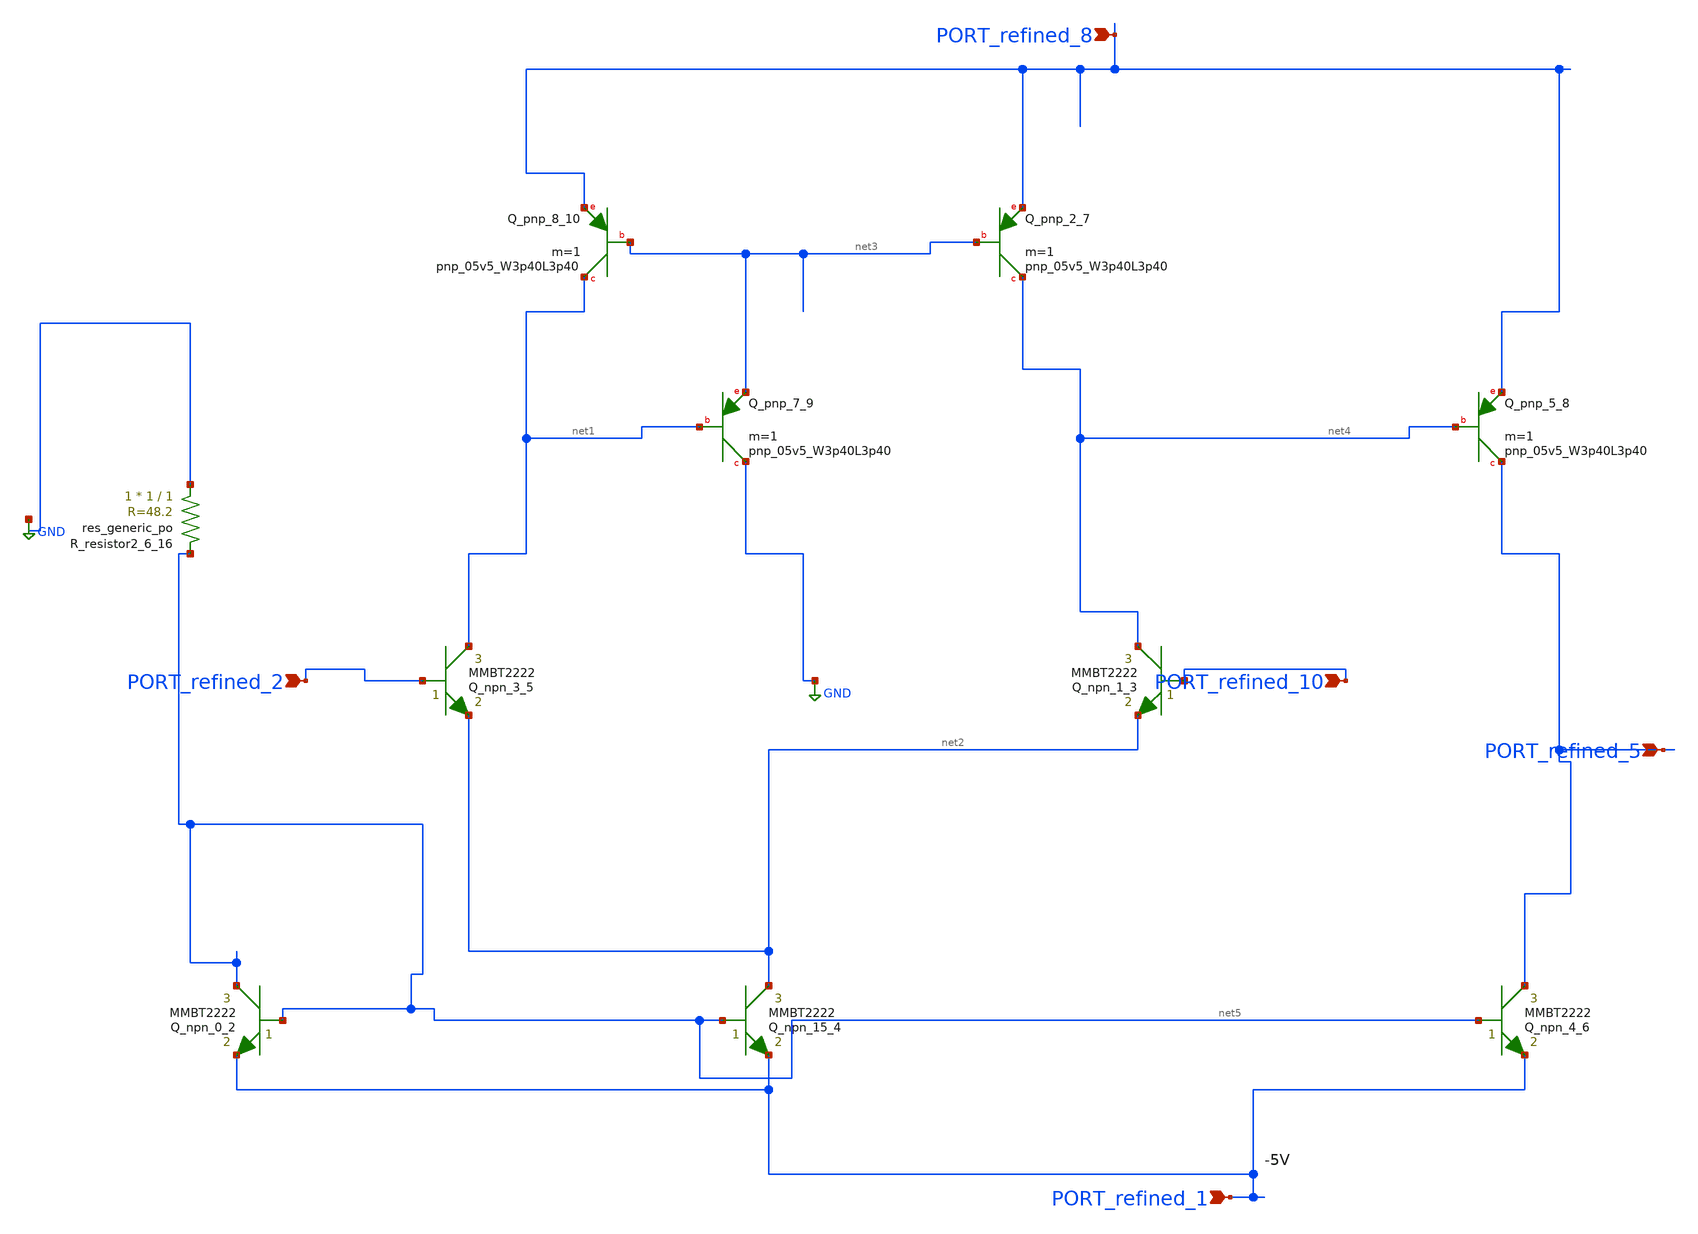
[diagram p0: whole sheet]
** sch_path: schematics/Image2Net/060.sch
**.subckt 060 PORT_refined_8 PORT_refined_10 PORT_refined_2 PORT_refined_5 PORT_refined_1
*.ipin PORT_refined_8
*.ipin PORT_refined_10
*.ipin PORT_refined_2
*.ipin PORT_refined_5
*.ipin PORT_refined_1
Q_npn_0_2 net5 net5 PORT_refined_1 MMBT2222 area=1 m=1
Q_npn_1_3 net4 PORT_refined_10 net2 MMBT2222 area=1 m=1
Q_npn_15_4 net2 net5 PORT_refined_1 MMBT2222 area=1 m=1
Q_npn_3_5 net1 PORT_refined_2 net2 MMBT2222 area=1 m=1
Q_npn_4_6 PORT_refined_5 net5 PORT_refined_1 MMBT2222 area=1 m=1
XQ_pnp_2_7 net4 net3 PORT_refined_8 sky130_fd_pr__pnp_05v5_W3p40L3p40 m=1
XQ_pnp_5_8 PORT_refined_5 net4 PORT_refined_8 sky130_fd_pr__pnp_05v5_W3p40L3p40 m=1
XQ_pnp_7_9 GND net1 net3 sky130_fd_pr__pnp_05v5_W3p40L3p40 m=1
XQ_pnp_8_10 net1 net3 PORT_refined_8 sky130_fd_pr__pnp_05v5_W3p40L3p40 m=1
XR_resistor2_6_16 GND net5 sky130_fd_pr__res_generic_po W=1 L=1 m=1
**.ends
.GLOBAL GND
.end
